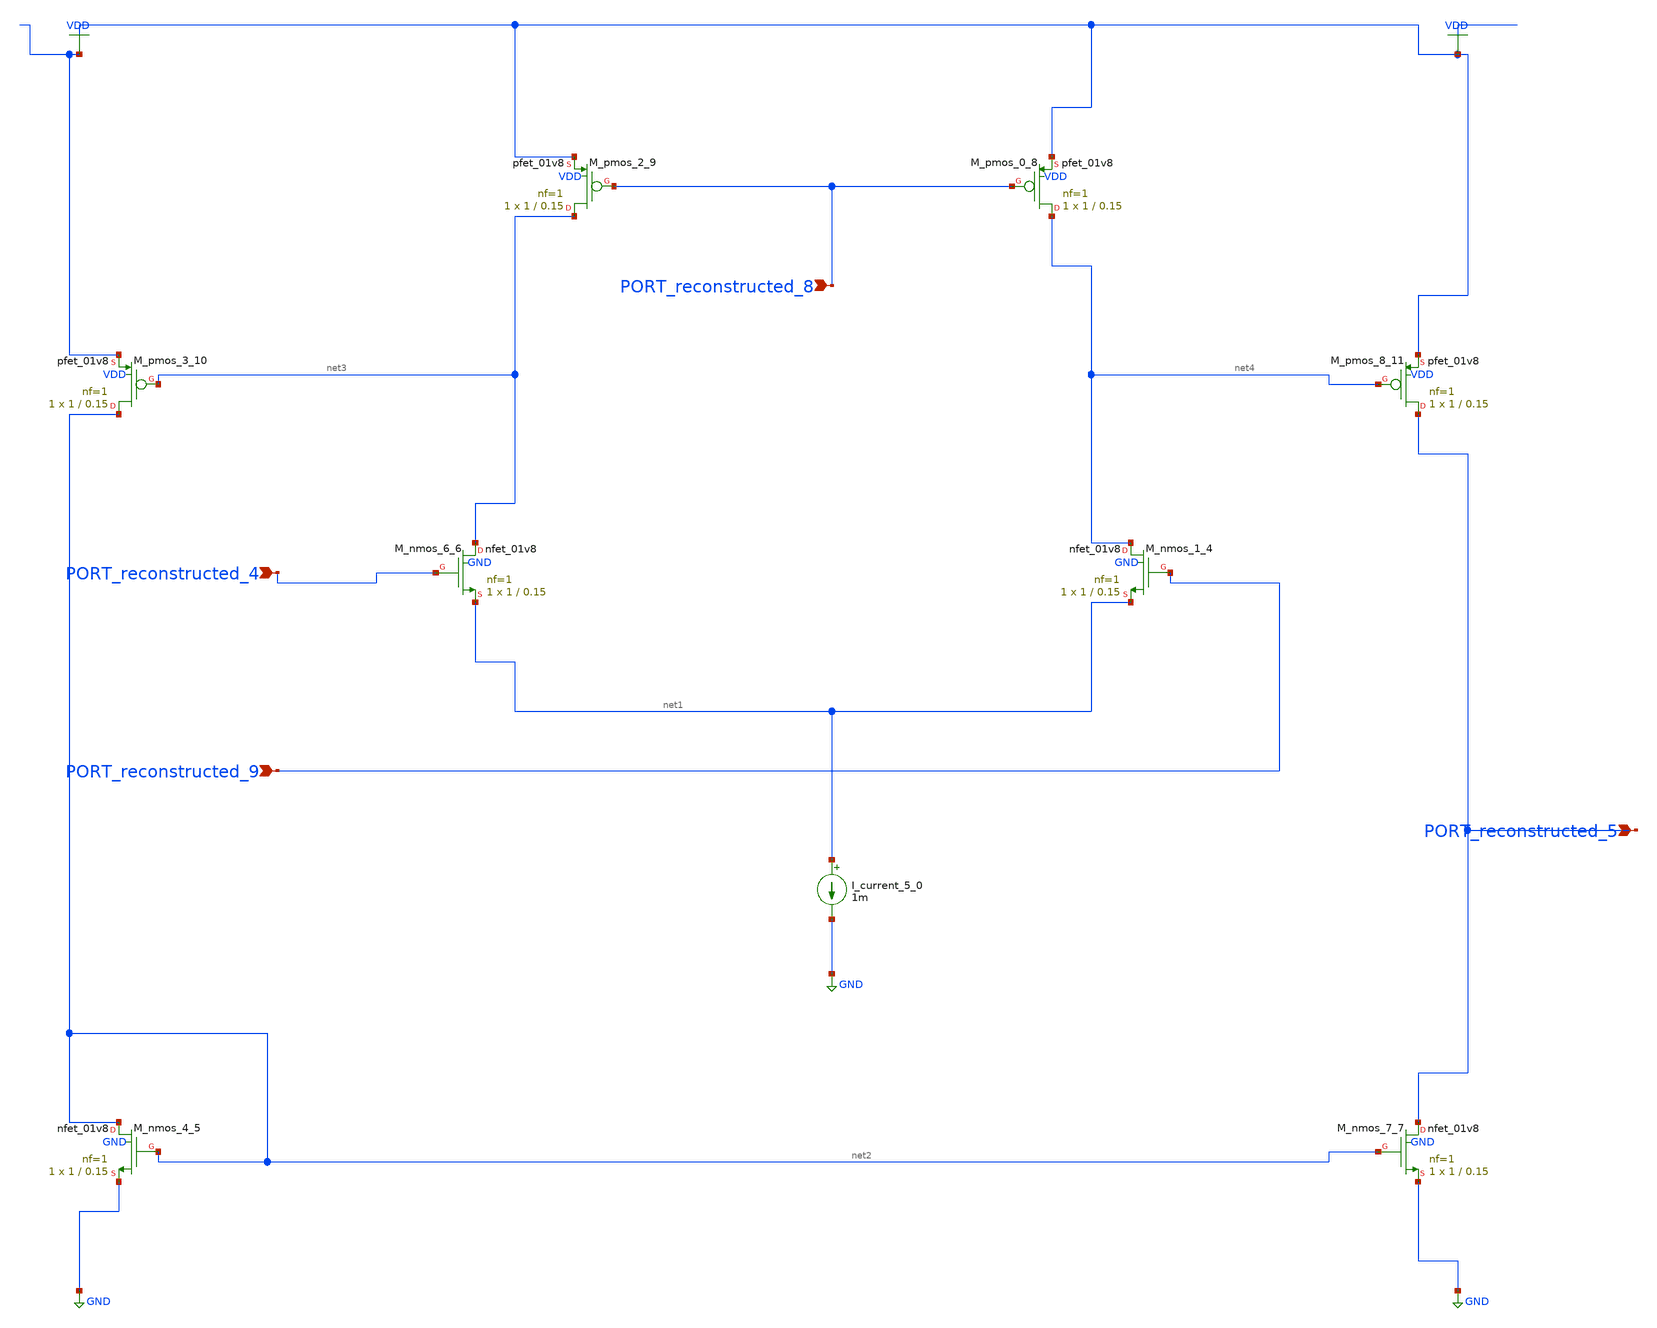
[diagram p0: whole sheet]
** sch_path: schematics/AMSNet/647.sch
**.subckt 647 PORT_reconstructed_5 PORT_reconstructed_4 PORT_reconstructed_9 PORT_reconstructed_8
*.ipin PORT_reconstructed_5
*.ipin PORT_reconstructed_4
*.ipin PORT_reconstructed_9
*.ipin PORT_reconstructed_8
I_current_5_0 net1 GND 1m
XM_nmos_1_4 net4 PORT_reconstructed_9 net1 GND sky130_fd_pr__nfet_01v8 L=0.15 W=1 nf=1 ad='int((1 + 1)/2) * 1 / 1 * 0.29'
+ as='int((1 + 2)/2) * 1 / 1 * 0.29' pd='2*int((1 + 1)/2) * (1 / 1 + 0.29)' ps='2*int((1 + 2)/2) * (1 / 1 + 0.29)'
+ nrd='0.29 / 1 ' nrs='0.29 / 1 ' sa=0 sb=0 sd=0 mult=1 m=1
XM_nmos_4_5 net2 net2 GND GND sky130_fd_pr__nfet_01v8 L=0.15 W=1 nf=1 ad='int((1 + 1)/2) * 1 / 1 * 0.29'
+ as='int((1 + 2)/2) * 1 / 1 * 0.29' pd='2*int((1 + 1)/2) * (1 / 1 + 0.29)' ps='2*int((1 + 2)/2) * (1 / 1 + 0.29)'
+ nrd='0.29 / 1 ' nrs='0.29 / 1 ' sa=0 sb=0 sd=0 mult=1 m=1
XM_nmos_6_6 net3 PORT_reconstructed_4 net1 GND sky130_fd_pr__nfet_01v8 L=0.15 W=1 nf=1 ad='int((1 + 1)/2) * 1 / 1 * 0.29'
+ as='int((1 + 2)/2) * 1 / 1 * 0.29' pd='2*int((1 + 1)/2) * (1 / 1 + 0.29)' ps='2*int((1 + 2)/2) * (1 / 1 + 0.29)'
+ nrd='0.29 / 1 ' nrs='0.29 / 1 ' sa=0 sb=0 sd=0 mult=1 m=1
XM_nmos_7_7 PORT_reconstructed_5 net2 GND GND sky130_fd_pr__nfet_01v8 L=0.15 W=1 nf=1 ad='int((1 + 1)/2) * 1 / 1 * 0.29'
+ as='int((1 + 2)/2) * 1 / 1 * 0.29' pd='2*int((1 + 1)/2) * (1 / 1 + 0.29)' ps='2*int((1 + 2)/2) * (1 / 1 + 0.29)'
+ nrd='0.29 / 1 ' nrs='0.29 / 1 ' sa=0 sb=0 sd=0 mult=1 m=1
XM_pmos_0_8 net4 PORT_reconstructed_8 VDD VDD sky130_fd_pr__pfet_01v8 L=0.15 W=1 nf=1 ad='int((1 + 1)/2) * 1 / 1 * 0.29'
+ as='int((1 + 2)/2) * 1 / 1 * 0.29' pd='2*int((1 + 1)/2) * (1 / 1 + 0.29)' ps='2*int((1 + 2)/2) * (1 / 1 + 0.29)'
+ nrd='0.29 / 1 ' nrs='0.29 / 1 ' sa=0 sb=0 sd=0 mult=1 m=1
XM_pmos_2_9 net3 PORT_reconstructed_8 VDD VDD sky130_fd_pr__pfet_01v8 L=0.15 W=1 nf=1 ad='int((1 + 1)/2) * 1 / 1 * 0.29'
+ as='int((1 + 2)/2) * 1 / 1 * 0.29' pd='2*int((1 + 1)/2) * (1 / 1 + 0.29)' ps='2*int((1 + 2)/2) * (1 / 1 + 0.29)'
+ nrd='0.29 / 1 ' nrs='0.29 / 1 ' sa=0 sb=0 sd=0 mult=1 m=1
XM_pmos_3_10 net2 net3 VDD VDD sky130_fd_pr__pfet_01v8 L=0.15 W=1 nf=1 ad='int((1 + 1)/2) * 1 / 1 * 0.29'
+ as='int((1 + 2)/2) * 1 / 1 * 0.29' pd='2*int((1 + 1)/2) * (1 / 1 + 0.29)' ps='2*int((1 + 2)/2) * (1 / 1 + 0.29)'
+ nrd='0.29 / 1 ' nrs='0.29 / 1 ' sa=0 sb=0 sd=0 mult=1 m=1
XM_pmos_8_11 PORT_reconstructed_5 net4 VDD VDD sky130_fd_pr__pfet_01v8 L=0.15 W=1 nf=1 ad='int((1 + 1)/2) * 1 / 1 * 0.29'
+ as='int((1 + 2)/2) * 1 / 1 * 0.29' pd='2*int((1 + 1)/2) * (1 / 1 + 0.29)' ps='2*int((1 + 2)/2) * (1 / 1 + 0.29)'
+ nrd='0.29 / 1 ' nrs='0.29 / 1 ' sa=0 sb=0 sd=0 mult=1 m=1
**.ends
.GLOBAL GND
.GLOBAL VDD
.end
